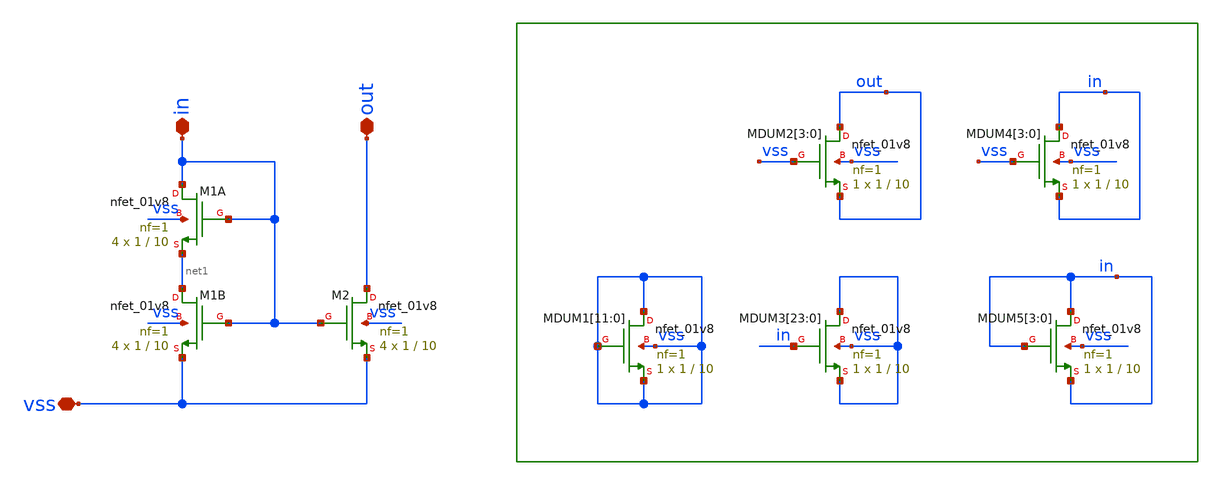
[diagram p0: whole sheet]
** sch_path: xschem/support/cmirr.sch
**.subckt cmirr vss in out
*.iopin vss
*.iopin in
*.iopin out
XM1B net1 in vss vss sky130_fd_pr__nfet_01v8 L=10 W=1 nf=1 ad='int((nf+1)/2) * W/nf * 0.29' as='int((nf+2)/2) * W/nf * 0.29'
+ pd='2*int((nf+1)/2) * (W/nf + 0.29)' ps='2*int((nf+2)/2) * (W/nf + 0.29)' nrd='0.29 / W' nrs='0.29 / W'
+ sa=0 sb=0 sd=0 mult=4 m=4
XM2 out in vss vss sky130_fd_pr__nfet_01v8 L=10 W=1 nf=1 ad='int((nf+1)/2) * W/nf * 0.29' as='int((nf+2)/2) * W/nf * 0.29'
+ pd='2*int((nf+1)/2) * (W/nf + 0.29)' ps='2*int((nf+2)/2) * (W/nf + 0.29)' nrd='0.29 / W' nrs='0.29 / W'
+ sa=0 sb=0 sd=0 mult=4 m=4
XM1A in in net1 vss sky130_fd_pr__nfet_01v8 L=10 W=1 nf=1 ad='int((nf+1)/2) * W/nf * 0.29' as='int((nf+2)/2) * W/nf * 0.29'
+ pd='2*int((nf+1)/2) * (W/nf + 0.29)' ps='2*int((nf+2)/2) * (W/nf + 0.29)' nrd='0.29 / W' nrs='0.29 / W'
+ sa=0 sb=0 sd=0 mult=4 m=4
XMDUM1[11] vss vss vss vss sky130_fd_pr__nfet_01v8 L=10 W=1 nf=1 ad='int((nf+1)/2) * W/nf * 0.29' as='int((nf+2)/2) * W/nf * 0.29'
+ pd='2*int((nf+1)/2) * (W/nf + 0.29)' ps='2*int((nf+2)/2) * (W/nf + 0.29)' nrd='0.29 / W' nrs='0.29 / W'
+ sa=0 sb=0 sd=0 mult=1 m=1
XMDUM1[10] vss vss vss vss sky130_fd_pr__nfet_01v8 L=10 W=1 nf=1 ad='int((nf+1)/2) * W/nf * 0.29' as='int((nf+2)/2) * W/nf * 0.29'
+ pd='2*int((nf+1)/2) * (W/nf + 0.29)' ps='2*int((nf+2)/2) * (W/nf + 0.29)' nrd='0.29 / W' nrs='0.29 / W'
+ sa=0 sb=0 sd=0 mult=1 m=1
XMDUM1[9] vss vss vss vss sky130_fd_pr__nfet_01v8 L=10 W=1 nf=1 ad='int((nf+1)/2) * W/nf * 0.29' as='int((nf+2)/2) * W/nf * 0.29'
+ pd='2*int((nf+1)/2) * (W/nf + 0.29)' ps='2*int((nf+2)/2) * (W/nf + 0.29)' nrd='0.29 / W' nrs='0.29 / W'
+ sa=0 sb=0 sd=0 mult=1 m=1
XMDUM1[8] vss vss vss vss sky130_fd_pr__nfet_01v8 L=10 W=1 nf=1 ad='int((nf+1)/2) * W/nf * 0.29' as='int((nf+2)/2) * W/nf * 0.29'
+ pd='2*int((nf+1)/2) * (W/nf + 0.29)' ps='2*int((nf+2)/2) * (W/nf + 0.29)' nrd='0.29 / W' nrs='0.29 / W'
+ sa=0 sb=0 sd=0 mult=1 m=1
XMDUM1[7] vss vss vss vss sky130_fd_pr__nfet_01v8 L=10 W=1 nf=1 ad='int((nf+1)/2) * W/nf * 0.29' as='int((nf+2)/2) * W/nf * 0.29'
+ pd='2*int((nf+1)/2) * (W/nf + 0.29)' ps='2*int((nf+2)/2) * (W/nf + 0.29)' nrd='0.29 / W' nrs='0.29 / W'
+ sa=0 sb=0 sd=0 mult=1 m=1
XMDUM1[6] vss vss vss vss sky130_fd_pr__nfet_01v8 L=10 W=1 nf=1 ad='int((nf+1)/2) * W/nf * 0.29' as='int((nf+2)/2) * W/nf * 0.29'
+ pd='2*int((nf+1)/2) * (W/nf + 0.29)' ps='2*int((nf+2)/2) * (W/nf + 0.29)' nrd='0.29 / W' nrs='0.29 / W'
+ sa=0 sb=0 sd=0 mult=1 m=1
XMDUM1[5] vss vss vss vss sky130_fd_pr__nfet_01v8 L=10 W=1 nf=1 ad='int((nf+1)/2) * W/nf * 0.29' as='int((nf+2)/2) * W/nf * 0.29'
+ pd='2*int((nf+1)/2) * (W/nf + 0.29)' ps='2*int((nf+2)/2) * (W/nf + 0.29)' nrd='0.29 / W' nrs='0.29 / W'
+ sa=0 sb=0 sd=0 mult=1 m=1
XMDUM1[4] vss vss vss vss sky130_fd_pr__nfet_01v8 L=10 W=1 nf=1 ad='int((nf+1)/2) * W/nf * 0.29' as='int((nf+2)/2) * W/nf * 0.29'
+ pd='2*int((nf+1)/2) * (W/nf + 0.29)' ps='2*int((nf+2)/2) * (W/nf + 0.29)' nrd='0.29 / W' nrs='0.29 / W'
+ sa=0 sb=0 sd=0 mult=1 m=1
XMDUM1[3] vss vss vss vss sky130_fd_pr__nfet_01v8 L=10 W=1 nf=1 ad='int((nf+1)/2) * W/nf * 0.29' as='int((nf+2)/2) * W/nf * 0.29'
+ pd='2*int((nf+1)/2) * (W/nf + 0.29)' ps='2*int((nf+2)/2) * (W/nf + 0.29)' nrd='0.29 / W' nrs='0.29 / W'
+ sa=0 sb=0 sd=0 mult=1 m=1
XMDUM1[2] vss vss vss vss sky130_fd_pr__nfet_01v8 L=10 W=1 nf=1 ad='int((nf+1)/2) * W/nf * 0.29' as='int((nf+2)/2) * W/nf * 0.29'
+ pd='2*int((nf+1)/2) * (W/nf + 0.29)' ps='2*int((nf+2)/2) * (W/nf + 0.29)' nrd='0.29 / W' nrs='0.29 / W'
+ sa=0 sb=0 sd=0 mult=1 m=1
XMDUM1[1] vss vss vss vss sky130_fd_pr__nfet_01v8 L=10 W=1 nf=1 ad='int((nf+1)/2) * W/nf * 0.29' as='int((nf+2)/2) * W/nf * 0.29'
+ pd='2*int((nf+1)/2) * (W/nf + 0.29)' ps='2*int((nf+2)/2) * (W/nf + 0.29)' nrd='0.29 / W' nrs='0.29 / W'
+ sa=0 sb=0 sd=0 mult=1 m=1
XMDUM1[0] vss vss vss vss sky130_fd_pr__nfet_01v8 L=10 W=1 nf=1 ad='int((nf+1)/2) * W/nf * 0.29' as='int((nf+2)/2) * W/nf * 0.29'
+ pd='2*int((nf+1)/2) * (W/nf + 0.29)' ps='2*int((nf+2)/2) * (W/nf + 0.29)' nrd='0.29 / W' nrs='0.29 / W'
+ sa=0 sb=0 sd=0 mult=1 m=1
XMDUM3[23] vss in vss vss sky130_fd_pr__nfet_01v8 L=10 W=1 nf=1 ad='int((nf+1)/2) * W/nf * 0.29' as='int((nf+2)/2) * W/nf * 0.29'
+ pd='2*int((nf+1)/2) * (W/nf + 0.29)' ps='2*int((nf+2)/2) * (W/nf + 0.29)' nrd='0.29 / W' nrs='0.29 / W'
+ sa=0 sb=0 sd=0 mult=1 m=1
XMDUM3[22] vss in vss vss sky130_fd_pr__nfet_01v8 L=10 W=1 nf=1 ad='int((nf+1)/2) * W/nf * 0.29' as='int((nf+2)/2) * W/nf * 0.29'
+ pd='2*int((nf+1)/2) * (W/nf + 0.29)' ps='2*int((nf+2)/2) * (W/nf + 0.29)' nrd='0.29 / W' nrs='0.29 / W'
+ sa=0 sb=0 sd=0 mult=1 m=1
XMDUM3[21] vss in vss vss sky130_fd_pr__nfet_01v8 L=10 W=1 nf=1 ad='int((nf+1)/2) * W/nf * 0.29' as='int((nf+2)/2) * W/nf * 0.29'
+ pd='2*int((nf+1)/2) * (W/nf + 0.29)' ps='2*int((nf+2)/2) * (W/nf + 0.29)' nrd='0.29 / W' nrs='0.29 / W'
+ sa=0 sb=0 sd=0 mult=1 m=1
XMDUM3[20] vss in vss vss sky130_fd_pr__nfet_01v8 L=10 W=1 nf=1 ad='int((nf+1)/2) * W/nf * 0.29' as='int((nf+2)/2) * W/nf * 0.29'
+ pd='2*int((nf+1)/2) * (W/nf + 0.29)' ps='2*int((nf+2)/2) * (W/nf + 0.29)' nrd='0.29 / W' nrs='0.29 / W'
+ sa=0 sb=0 sd=0 mult=1 m=1
XMDUM3[19] vss in vss vss sky130_fd_pr__nfet_01v8 L=10 W=1 nf=1 ad='int((nf+1)/2) * W/nf * 0.29' as='int((nf+2)/2) * W/nf * 0.29'
+ pd='2*int((nf+1)/2) * (W/nf + 0.29)' ps='2*int((nf+2)/2) * (W/nf + 0.29)' nrd='0.29 / W' nrs='0.29 / W'
+ sa=0 sb=0 sd=0 mult=1 m=1
XMDUM3[18] vss in vss vss sky130_fd_pr__nfet_01v8 L=10 W=1 nf=1 ad='int((nf+1)/2) * W/nf * 0.29' as='int((nf+2)/2) * W/nf * 0.29'
+ pd='2*int((nf+1)/2) * (W/nf + 0.29)' ps='2*int((nf+2)/2) * (W/nf + 0.29)' nrd='0.29 / W' nrs='0.29 / W'
+ sa=0 sb=0 sd=0 mult=1 m=1
XMDUM3[17] vss in vss vss sky130_fd_pr__nfet_01v8 L=10 W=1 nf=1 ad='int((nf+1)/2) * W/nf * 0.29' as='int((nf+2)/2) * W/nf * 0.29'
+ pd='2*int((nf+1)/2) * (W/nf + 0.29)' ps='2*int((nf+2)/2) * (W/nf + 0.29)' nrd='0.29 / W' nrs='0.29 / W'
+ sa=0 sb=0 sd=0 mult=1 m=1
XMDUM3[16] vss in vss vss sky130_fd_pr__nfet_01v8 L=10 W=1 nf=1 ad='int((nf+1)/2) * W/nf * 0.29' as='int((nf+2)/2) * W/nf * 0.29'
+ pd='2*int((nf+1)/2) * (W/nf + 0.29)' ps='2*int((nf+2)/2) * (W/nf + 0.29)' nrd='0.29 / W' nrs='0.29 / W'
+ sa=0 sb=0 sd=0 mult=1 m=1
XMDUM3[15] vss in vss vss sky130_fd_pr__nfet_01v8 L=10 W=1 nf=1 ad='int((nf+1)/2) * W/nf * 0.29' as='int((nf+2)/2) * W/nf * 0.29'
+ pd='2*int((nf+1)/2) * (W/nf + 0.29)' ps='2*int((nf+2)/2) * (W/nf + 0.29)' nrd='0.29 / W' nrs='0.29 / W'
+ sa=0 sb=0 sd=0 mult=1 m=1
XMDUM3[14] vss in vss vss sky130_fd_pr__nfet_01v8 L=10 W=1 nf=1 ad='int((nf+1)/2) * W/nf * 0.29' as='int((nf+2)/2) * W/nf * 0.29'
+ pd='2*int((nf+1)/2) * (W/nf + 0.29)' ps='2*int((nf+2)/2) * (W/nf + 0.29)' nrd='0.29 / W' nrs='0.29 / W'
+ sa=0 sb=0 sd=0 mult=1 m=1
XMDUM3[13] vss in vss vss sky130_fd_pr__nfet_01v8 L=10 W=1 nf=1 ad='int((nf+1)/2) * W/nf * 0.29' as='int((nf+2)/2) * W/nf * 0.29'
+ pd='2*int((nf+1)/2) * (W/nf + 0.29)' ps='2*int((nf+2)/2) * (W/nf + 0.29)' nrd='0.29 / W' nrs='0.29 / W'
+ sa=0 sb=0 sd=0 mult=1 m=1
XMDUM3[12] vss in vss vss sky130_fd_pr__nfet_01v8 L=10 W=1 nf=1 ad='int((nf+1)/2) * W/nf * 0.29' as='int((nf+2)/2) * W/nf * 0.29'
+ pd='2*int((nf+1)/2) * (W/nf + 0.29)' ps='2*int((nf+2)/2) * (W/nf + 0.29)' nrd='0.29 / W' nrs='0.29 / W'
+ sa=0 sb=0 sd=0 mult=1 m=1
XMDUM3[11] vss in vss vss sky130_fd_pr__nfet_01v8 L=10 W=1 nf=1 ad='int((nf+1)/2) * W/nf * 0.29' as='int((nf+2)/2) * W/nf * 0.29'
+ pd='2*int((nf+1)/2) * (W/nf + 0.29)' ps='2*int((nf+2)/2) * (W/nf + 0.29)' nrd='0.29 / W' nrs='0.29 / W'
+ sa=0 sb=0 sd=0 mult=1 m=1
XMDUM3[10] vss in vss vss sky130_fd_pr__nfet_01v8 L=10 W=1 nf=1 ad='int((nf+1)/2) * W/nf * 0.29' as='int((nf+2)/2) * W/nf * 0.29'
+ pd='2*int((nf+1)/2) * (W/nf + 0.29)' ps='2*int((nf+2)/2) * (W/nf + 0.29)' nrd='0.29 / W' nrs='0.29 / W'
+ sa=0 sb=0 sd=0 mult=1 m=1
XMDUM3[9] vss in vss vss sky130_fd_pr__nfet_01v8 L=10 W=1 nf=1 ad='int((nf+1)/2) * W/nf * 0.29' as='int((nf+2)/2) * W/nf * 0.29'
+ pd='2*int((nf+1)/2) * (W/nf + 0.29)' ps='2*int((nf+2)/2) * (W/nf + 0.29)' nrd='0.29 / W' nrs='0.29 / W'
+ sa=0 sb=0 sd=0 mult=1 m=1
XMDUM3[8] vss in vss vss sky130_fd_pr__nfet_01v8 L=10 W=1 nf=1 ad='int((nf+1)/2) * W/nf * 0.29' as='int((nf+2)/2) * W/nf * 0.29'
+ pd='2*int((nf+1)/2) * (W/nf + 0.29)' ps='2*int((nf+2)/2) * (W/nf + 0.29)' nrd='0.29 / W' nrs='0.29 / W'
+ sa=0 sb=0 sd=0 mult=1 m=1
XMDUM3[7] vss in vss vss sky130_fd_pr__nfet_01v8 L=10 W=1 nf=1 ad='int((nf+1)/2) * W/nf * 0.29' as='int((nf+2)/2) * W/nf * 0.29'
+ pd='2*int((nf+1)/2) * (W/nf + 0.29)' ps='2*int((nf+2)/2) * (W/nf + 0.29)' nrd='0.29 / W' nrs='0.29 / W'
+ sa=0 sb=0 sd=0 mult=1 m=1
XMDUM3[6] vss in vss vss sky130_fd_pr__nfet_01v8 L=10 W=1 nf=1 ad='int((nf+1)/2) * W/nf * 0.29' as='int((nf+2)/2) * W/nf * 0.29'
+ pd='2*int((nf+1)/2) * (W/nf + 0.29)' ps='2*int((nf+2)/2) * (W/nf + 0.29)' nrd='0.29 / W' nrs='0.29 / W'
+ sa=0 sb=0 sd=0 mult=1 m=1
XMDUM3[5] vss in vss vss sky130_fd_pr__nfet_01v8 L=10 W=1 nf=1 ad='int((nf+1)/2) * W/nf * 0.29' as='int((nf+2)/2) * W/nf * 0.29'
+ pd='2*int((nf+1)/2) * (W/nf + 0.29)' ps='2*int((nf+2)/2) * (W/nf + 0.29)' nrd='0.29 / W' nrs='0.29 / W'
+ sa=0 sb=0 sd=0 mult=1 m=1
XMDUM3[4] vss in vss vss sky130_fd_pr__nfet_01v8 L=10 W=1 nf=1 ad='int((nf+1)/2) * W/nf * 0.29' as='int((nf+2)/2) * W/nf * 0.29'
+ pd='2*int((nf+1)/2) * (W/nf + 0.29)' ps='2*int((nf+2)/2) * (W/nf + 0.29)' nrd='0.29 / W' nrs='0.29 / W'
+ sa=0 sb=0 sd=0 mult=1 m=1
XMDUM3[3] vss in vss vss sky130_fd_pr__nfet_01v8 L=10 W=1 nf=1 ad='int((nf+1)/2) * W/nf * 0.29' as='int((nf+2)/2) * W/nf * 0.29'
+ pd='2*int((nf+1)/2) * (W/nf + 0.29)' ps='2*int((nf+2)/2) * (W/nf + 0.29)' nrd='0.29 / W' nrs='0.29 / W'
+ sa=0 sb=0 sd=0 mult=1 m=1
XMDUM3[2] vss in vss vss sky130_fd_pr__nfet_01v8 L=10 W=1 nf=1 ad='int((nf+1)/2) * W/nf * 0.29' as='int((nf+2)/2) * W/nf * 0.29'
+ pd='2*int((nf+1)/2) * (W/nf + 0.29)' ps='2*int((nf+2)/2) * (W/nf + 0.29)' nrd='0.29 / W' nrs='0.29 / W'
+ sa=0 sb=0 sd=0 mult=1 m=1
XMDUM3[1] vss in vss vss sky130_fd_pr__nfet_01v8 L=10 W=1 nf=1 ad='int((nf+1)/2) * W/nf * 0.29' as='int((nf+2)/2) * W/nf * 0.29'
+ pd='2*int((nf+1)/2) * (W/nf + 0.29)' ps='2*int((nf+2)/2) * (W/nf + 0.29)' nrd='0.29 / W' nrs='0.29 / W'
+ sa=0 sb=0 sd=0 mult=1 m=1
XMDUM3[0] vss in vss vss sky130_fd_pr__nfet_01v8 L=10 W=1 nf=1 ad='int((nf+1)/2) * W/nf * 0.29' as='int((nf+2)/2) * W/nf * 0.29'
+ pd='2*int((nf+1)/2) * (W/nf + 0.29)' ps='2*int((nf+2)/2) * (W/nf + 0.29)' nrd='0.29 / W' nrs='0.29 / W'
+ sa=0 sb=0 sd=0 mult=1 m=1
XMDUM2[3] out vss out vss sky130_fd_pr__nfet_01v8 L=10 W=1 nf=1 ad='int((nf+1)/2) * W/nf * 0.29' as='int((nf+2)/2) * W/nf * 0.29'
+ pd='2*int((nf+1)/2) * (W/nf + 0.29)' ps='2*int((nf+2)/2) * (W/nf + 0.29)' nrd='0.29 / W' nrs='0.29 / W'
+ sa=0 sb=0 sd=0 mult=1 m=1
XMDUM2[2] out vss out vss sky130_fd_pr__nfet_01v8 L=10 W=1 nf=1 ad='int((nf+1)/2) * W/nf * 0.29' as='int((nf+2)/2) * W/nf * 0.29'
+ pd='2*int((nf+1)/2) * (W/nf + 0.29)' ps='2*int((nf+2)/2) * (W/nf + 0.29)' nrd='0.29 / W' nrs='0.29 / W'
+ sa=0 sb=0 sd=0 mult=1 m=1
XMDUM2[1] out vss out vss sky130_fd_pr__nfet_01v8 L=10 W=1 nf=1 ad='int((nf+1)/2) * W/nf * 0.29' as='int((nf+2)/2) * W/nf * 0.29'
+ pd='2*int((nf+1)/2) * (W/nf + 0.29)' ps='2*int((nf+2)/2) * (W/nf + 0.29)' nrd='0.29 / W' nrs='0.29 / W'
+ sa=0 sb=0 sd=0 mult=1 m=1
XMDUM2[0] out vss out vss sky130_fd_pr__nfet_01v8 L=10 W=1 nf=1 ad='int((nf+1)/2) * W/nf * 0.29' as='int((nf+2)/2) * W/nf * 0.29'
+ pd='2*int((nf+1)/2) * (W/nf + 0.29)' ps='2*int((nf+2)/2) * (W/nf + 0.29)' nrd='0.29 / W' nrs='0.29 / W'
+ sa=0 sb=0 sd=0 mult=1 m=1
XMDUM4[3] in vss in vss sky130_fd_pr__nfet_01v8 L=10 W=1 nf=1 ad='int((nf+1)/2) * W/nf * 0.29' as='int((nf+2)/2) * W/nf * 0.29'
+ pd='2*int((nf+1)/2) * (W/nf + 0.29)' ps='2*int((nf+2)/2) * (W/nf + 0.29)' nrd='0.29 / W' nrs='0.29 / W'
+ sa=0 sb=0 sd=0 mult=1 m=1
XMDUM4[2] in vss in vss sky130_fd_pr__nfet_01v8 L=10 W=1 nf=1 ad='int((nf+1)/2) * W/nf * 0.29' as='int((nf+2)/2) * W/nf * 0.29'
+ pd='2*int((nf+1)/2) * (W/nf + 0.29)' ps='2*int((nf+2)/2) * (W/nf + 0.29)' nrd='0.29 / W' nrs='0.29 / W'
+ sa=0 sb=0 sd=0 mult=1 m=1
XMDUM4[1] in vss in vss sky130_fd_pr__nfet_01v8 L=10 W=1 nf=1 ad='int((nf+1)/2) * W/nf * 0.29' as='int((nf+2)/2) * W/nf * 0.29'
+ pd='2*int((nf+1)/2) * (W/nf + 0.29)' ps='2*int((nf+2)/2) * (W/nf + 0.29)' nrd='0.29 / W' nrs='0.29 / W'
+ sa=0 sb=0 sd=0 mult=1 m=1
XMDUM4[0] in vss in vss sky130_fd_pr__nfet_01v8 L=10 W=1 nf=1 ad='int((nf+1)/2) * W/nf * 0.29' as='int((nf+2)/2) * W/nf * 0.29'
+ pd='2*int((nf+1)/2) * (W/nf + 0.29)' ps='2*int((nf+2)/2) * (W/nf + 0.29)' nrd='0.29 / W' nrs='0.29 / W'
+ sa=0 sb=0 sd=0 mult=1 m=1
XMDUM5[3] in in in vss sky130_fd_pr__nfet_01v8 L=10 W=1 nf=1 ad='int((nf+1)/2) * W/nf * 0.29' as='int((nf+2)/2) * W/nf * 0.29'
+ pd='2*int((nf+1)/2) * (W/nf + 0.29)' ps='2*int((nf+2)/2) * (W/nf + 0.29)' nrd='0.29 / W' nrs='0.29 / W'
+ sa=0 sb=0 sd=0 mult=1 m=1
XMDUM5[2] in in in vss sky130_fd_pr__nfet_01v8 L=10 W=1 nf=1 ad='int((nf+1)/2) * W/nf * 0.29' as='int((nf+2)/2) * W/nf * 0.29'
+ pd='2*int((nf+1)/2) * (W/nf + 0.29)' ps='2*int((nf+2)/2) * (W/nf + 0.29)' nrd='0.29 / W' nrs='0.29 / W'
+ sa=0 sb=0 sd=0 mult=1 m=1
XMDUM5[1] in in in vss sky130_fd_pr__nfet_01v8 L=10 W=1 nf=1 ad='int((nf+1)/2) * W/nf * 0.29' as='int((nf+2)/2) * W/nf * 0.29'
+ pd='2*int((nf+1)/2) * (W/nf + 0.29)' ps='2*int((nf+2)/2) * (W/nf + 0.29)' nrd='0.29 / W' nrs='0.29 / W'
+ sa=0 sb=0 sd=0 mult=1 m=1
XMDUM5[0] in in in vss sky130_fd_pr__nfet_01v8 L=10 W=1 nf=1 ad='int((nf+1)/2) * W/nf * 0.29' as='int((nf+2)/2) * W/nf * 0.29'
+ pd='2*int((nf+1)/2) * (W/nf + 0.29)' ps='2*int((nf+2)/2) * (W/nf + 0.29)' nrd='0.29 / W' nrs='0.29 / W'
+ sa=0 sb=0 sd=0 mult=1 m=1
**.ends
.end
